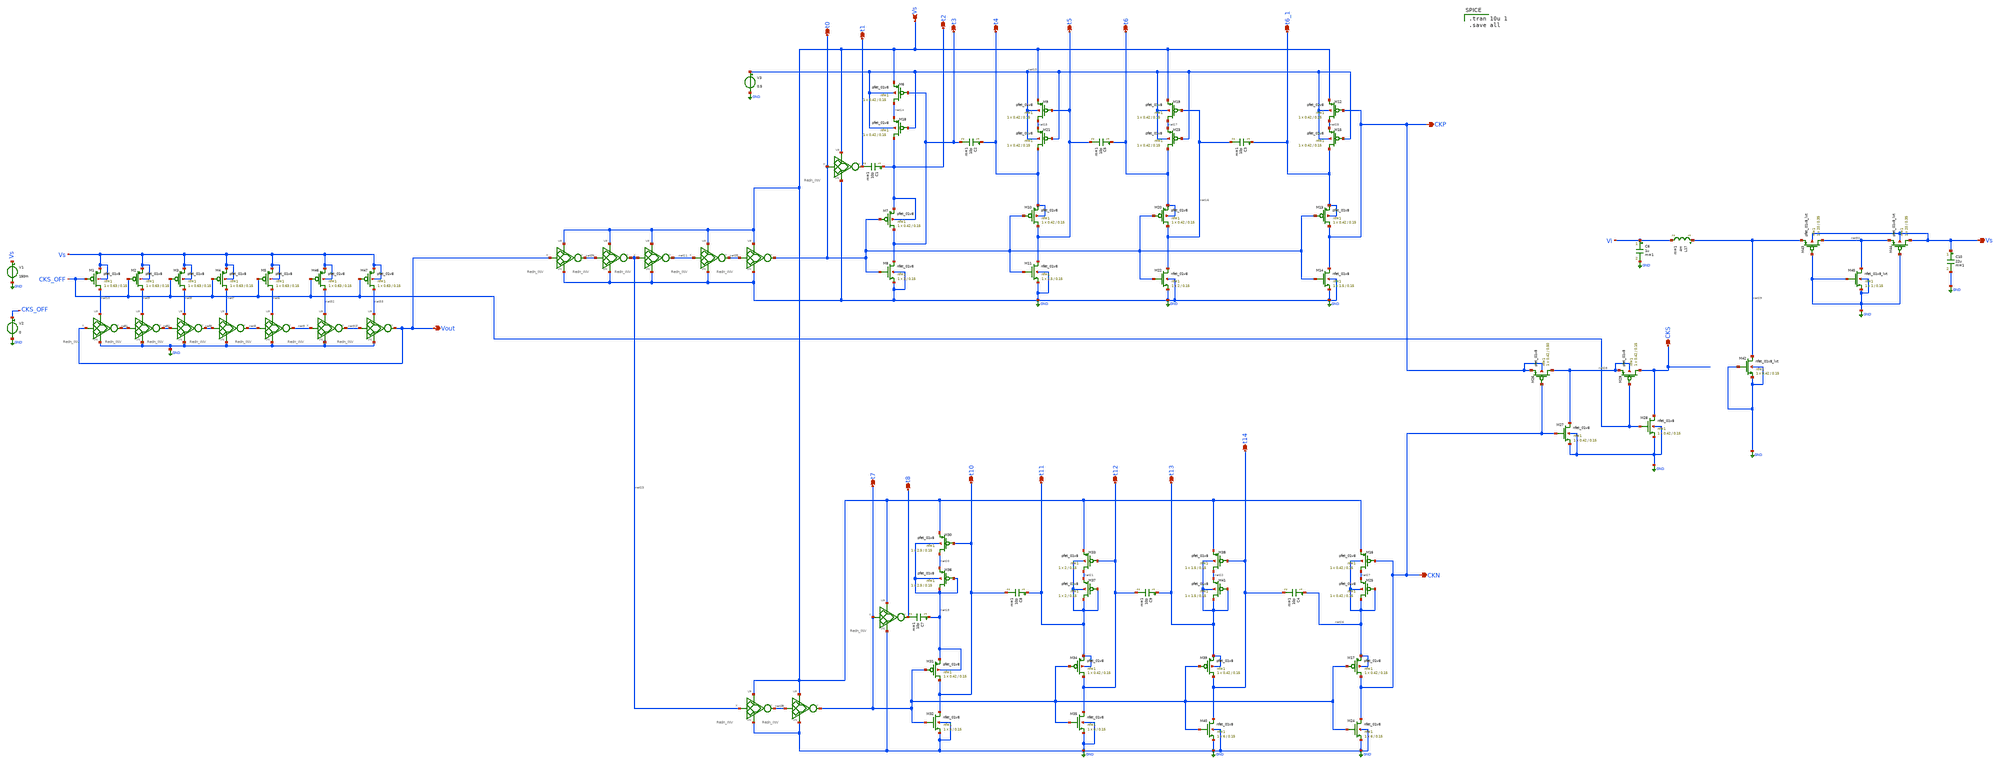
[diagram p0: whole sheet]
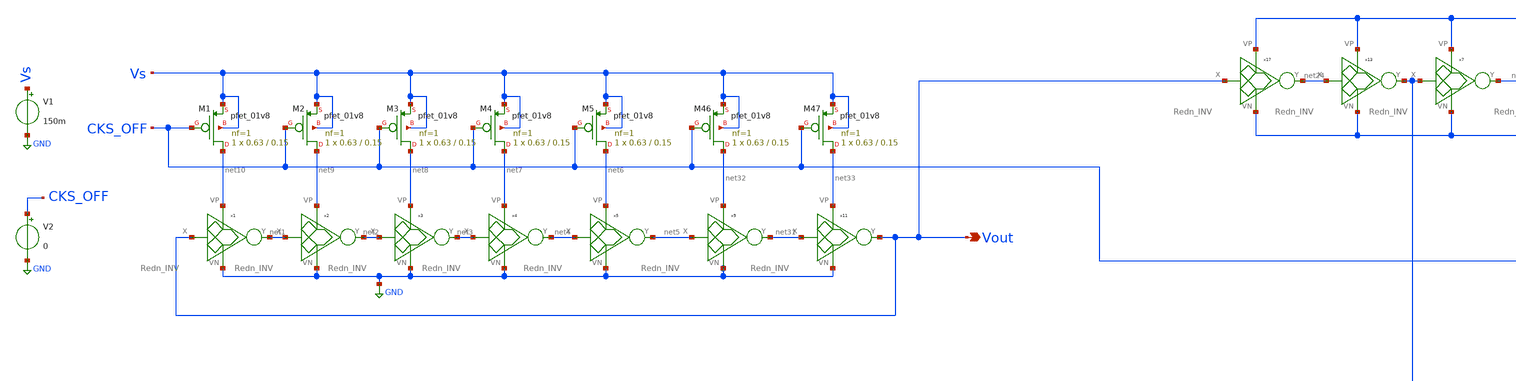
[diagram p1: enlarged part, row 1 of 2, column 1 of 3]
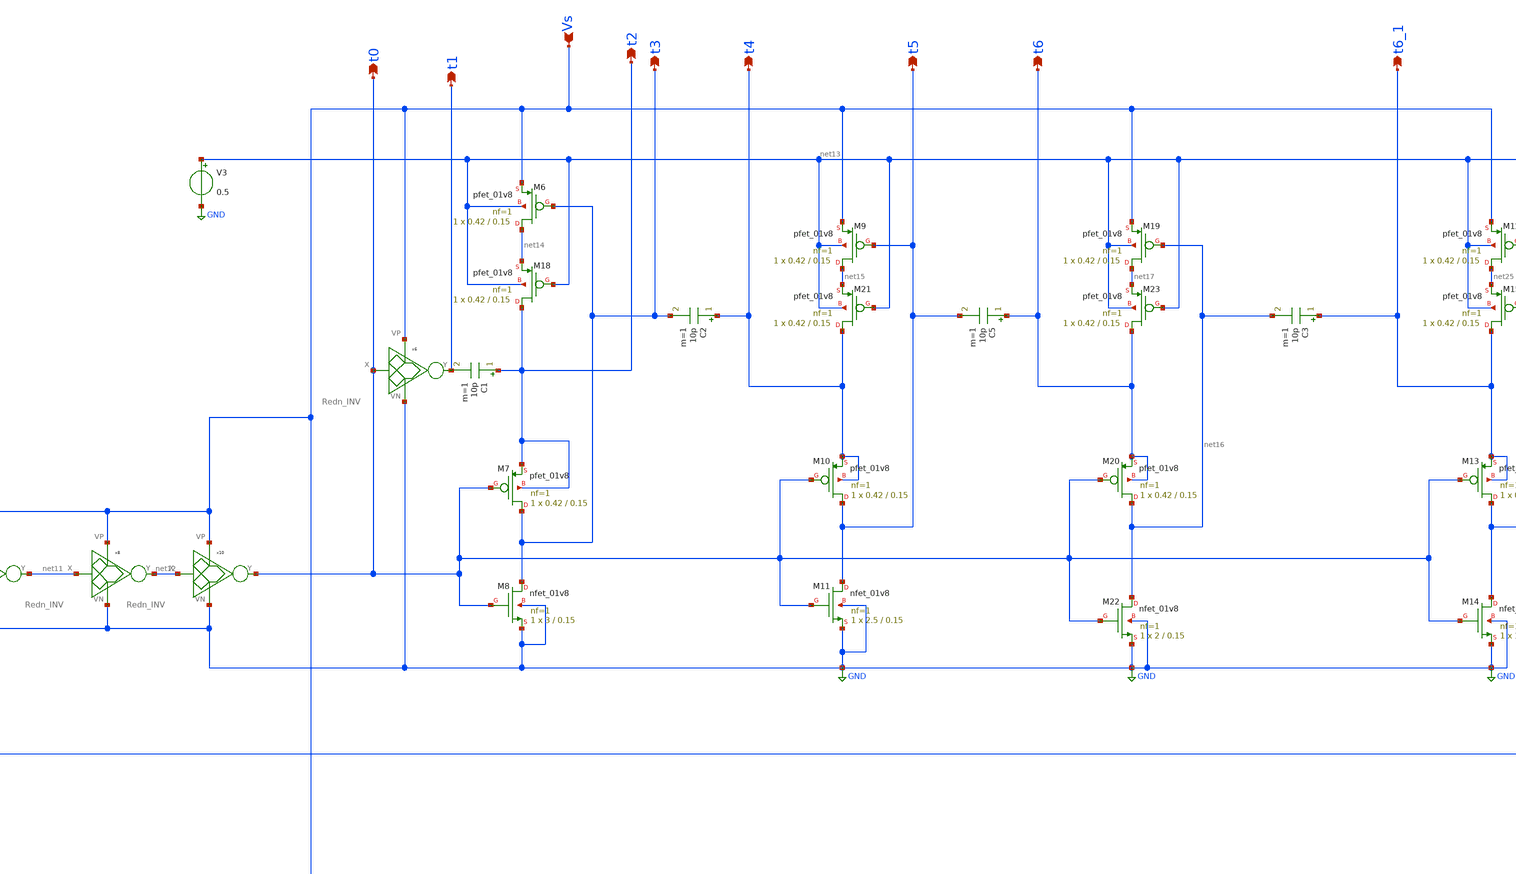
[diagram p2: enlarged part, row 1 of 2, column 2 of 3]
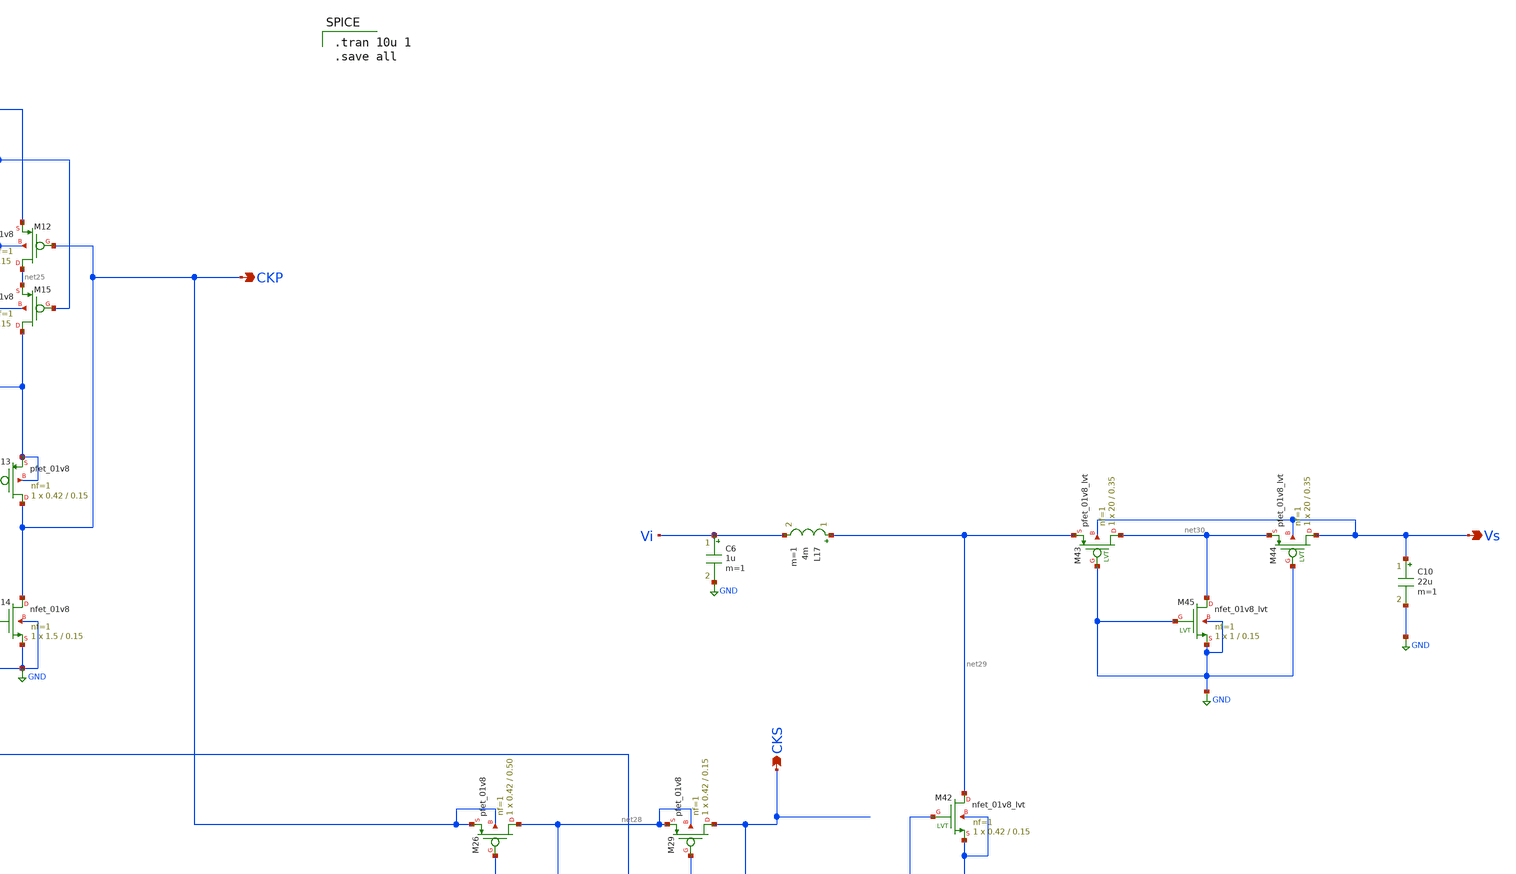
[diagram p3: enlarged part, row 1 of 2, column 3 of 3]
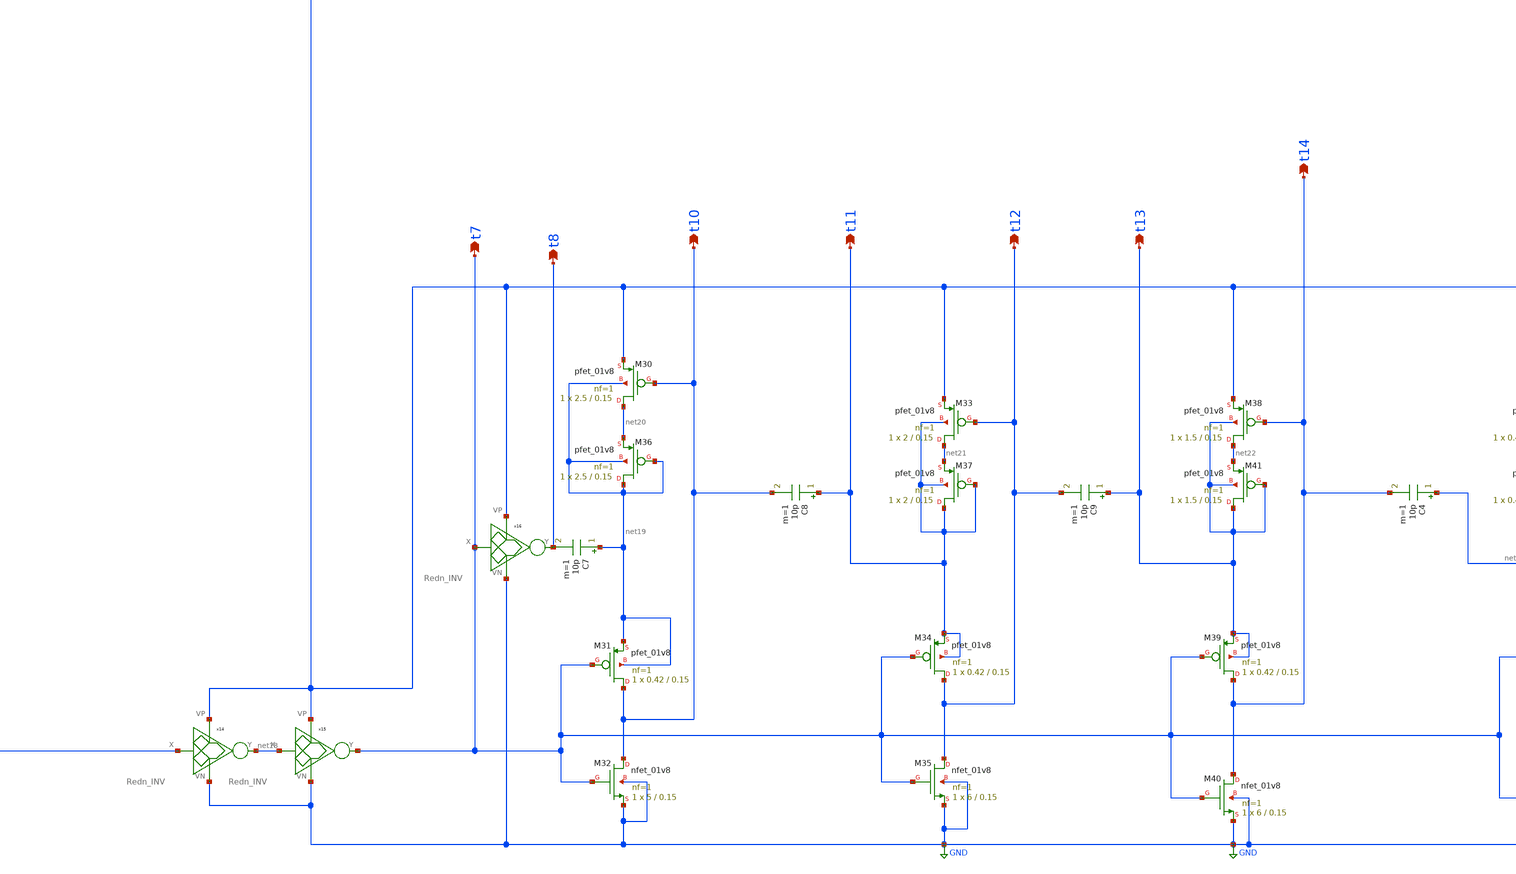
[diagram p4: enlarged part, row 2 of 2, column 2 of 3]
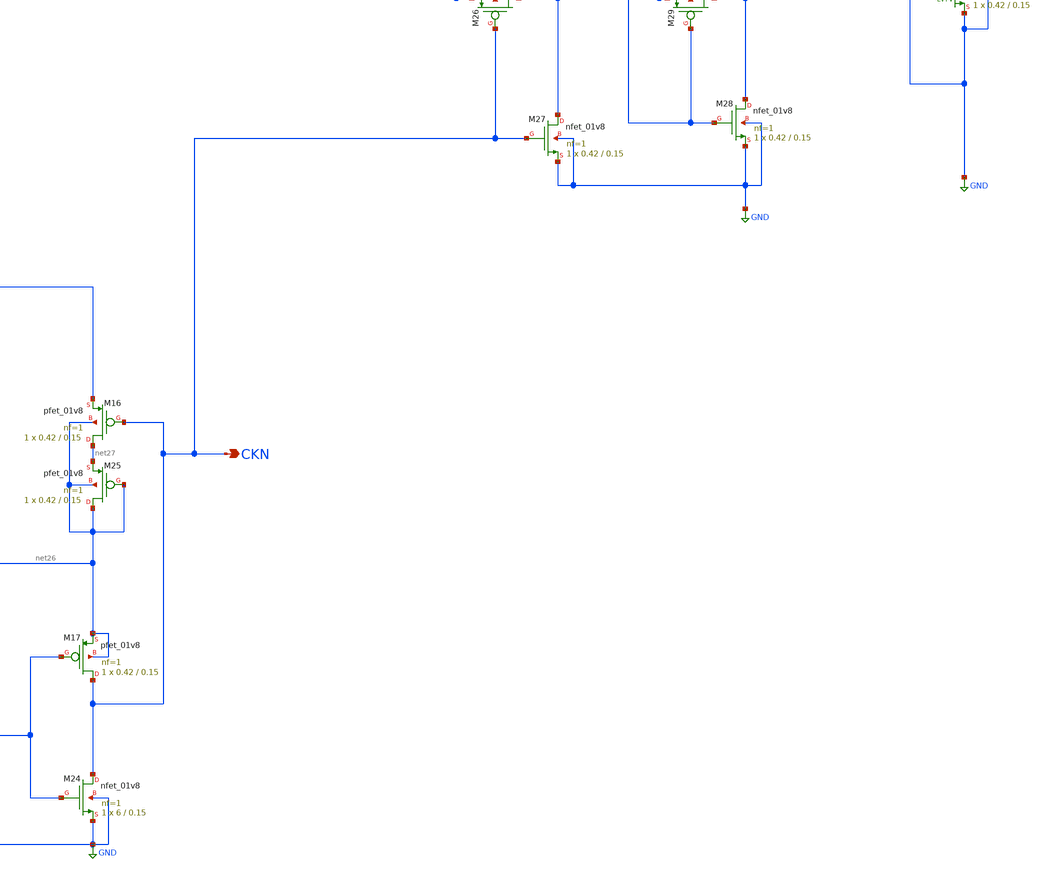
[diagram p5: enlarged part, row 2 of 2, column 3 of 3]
** sch_path: Blocks/Startup Converter/Startup_Conv_3.sch
**.subckt Startup_Conv_3 Vout Vs t2 t3 t4 t1 t0 t6 t5 t10 t11 t8 t7 t13 t12 CKP t6_1 CKN t14 CKS Vs
*.opin Vout
*.ipin Vs
*.opin t2
*.opin t3
*.opin t4
*.opin t1
*.opin t0
*.opin t6
*.opin t5
*.opin t10
*.opin t11
*.opin t8
*.opin t7
*.opin t13
*.opin t12
*.opin CKP
*.opin t6_1
*.opin CKN
*.opin t14
*.opin CKS
*.opin Vs
V1 Vs GND 150m
XM1 net10 CKS_OFF Vs Vs sky130_fd_pr__pfet_01v8 L=0.15 W=0.63 nf=1 ad='int((nf+1)/2) * W/nf * 0.29' as='int((nf+2)/2) * W/nf * 0.29'
+ pd='2*int((nf+1)/2) * (W/nf + 0.29)' ps='2*int((nf+2)/2) * (W/nf + 0.29)' nrd='0.29 / W' nrs='0.29 / W'
+ sa=0 sb=0 sd=0 mult=1 m=1
XM2 net9 CKS_OFF Vs Vs sky130_fd_pr__pfet_01v8 L=0.15 W=0.63 nf=1 ad='int((nf+1)/2) * W/nf * 0.29' as='int((nf+2)/2) * W/nf * 0.29'
+ pd='2*int((nf+1)/2) * (W/nf + 0.29)' ps='2*int((nf+2)/2) * (W/nf + 0.29)' nrd='0.29 / W' nrs='0.29 / W'
+ sa=0 sb=0 sd=0 mult=1 m=1
XM3 net8 CKS_OFF Vs Vs sky130_fd_pr__pfet_01v8 L=0.15 W=0.63 nf=1 ad='int((nf+1)/2) * W/nf * 0.29' as='int((nf+2)/2) * W/nf * 0.29'
+ pd='2*int((nf+1)/2) * (W/nf + 0.29)' ps='2*int((nf+2)/2) * (W/nf + 0.29)' nrd='0.29 / W' nrs='0.29 / W'
+ sa=0 sb=0 sd=0 mult=1 m=1
XM4 net7 CKS_OFF Vs Vs sky130_fd_pr__pfet_01v8 L=0.15 W=0.63 nf=1 ad='int((nf+1)/2) * W/nf * 0.29' as='int((nf+2)/2) * W/nf * 0.29'
+ pd='2*int((nf+1)/2) * (W/nf + 0.29)' ps='2*int((nf+2)/2) * (W/nf + 0.29)' nrd='0.29 / W' nrs='0.29 / W'
+ sa=0 sb=0 sd=0 mult=1 m=1
XM5 net6 CKS_OFF Vs Vs sky130_fd_pr__pfet_01v8 L=0.15 W=0.63 nf=1 ad='int((nf+1)/2) * W/nf * 0.29' as='int((nf+2)/2) * W/nf * 0.29'
+ pd='2*int((nf+1)/2) * (W/nf + 0.29)' ps='2*int((nf+2)/2) * (W/nf + 0.29)' nrd='0.29 / W' nrs='0.29 / W'
+ sa=0 sb=0 sd=0 mult=1 m=1
V2 CKS_OFF GND 0
x1 Vout net1 net10 GND Redn_INV
x2 net1 net2 net9 GND Redn_INV
x3 net2 net3 net8 GND Redn_INV
x4 net3 net4 net7 GND Redn_INV
x5 net4 net5 net6 GND Redn_INV
C1 t2 t1 10p m=1
XM6 net14 t3 Vs net13 sky130_fd_pr__pfet_01v8 L=0.15 W=0.42 nf=1 ad='int((nf+1)/2) * W/nf * 0.29' as='int((nf+2)/2) * W/nf * 0.29'
+ pd='2*int((nf+1)/2) * (W/nf + 0.29)' ps='2*int((nf+2)/2) * (W/nf + 0.29)' nrd='0.29 / W' nrs='0.29 / W'
+ sa=0 sb=0 sd=0 mult=1 m=1
XM7 t3 t0 t2 t2 sky130_fd_pr__pfet_01v8 L=0.15 W=0.42 nf=1 ad='int((nf+1)/2) * W/nf * 0.29' as='int((nf+2)/2) * W/nf * 0.29'
+ pd='2*int((nf+1)/2) * (W/nf + 0.29)' ps='2*int((nf+2)/2) * (W/nf + 0.29)' nrd='0.29 / W' nrs='0.29 / W'
+ sa=0 sb=0 sd=0 mult=1 m=1
XM8 t3 t0 GND GND sky130_fd_pr__nfet_01v8 L=0.15 W=3 nf=1 ad='int((nf+1)/2) * W/nf * 0.29' as='int((nf+2)/2) * W/nf * 0.29'
+ pd='2*int((nf+1)/2) * (W/nf + 0.29)' ps='2*int((nf+2)/2) * (W/nf + 0.29)' nrd='0.29 / W' nrs='0.29 / W'
+ sa=0 sb=0 sd=0 mult=1 m=1
XM9 net15 t5 Vs net13 sky130_fd_pr__pfet_01v8 L=0.15 W=0.42 nf=1 ad='int((nf+1)/2) * W/nf * 0.29' as='int((nf+2)/2) * W/nf * 0.29'
+ pd='2*int((nf+1)/2) * (W/nf + 0.29)' ps='2*int((nf+2)/2) * (W/nf + 0.29)' nrd='0.29 / W' nrs='0.29 / W'
+ sa=0 sb=0 sd=0 mult=1 m=1
XM10 t5 t0 t4 t4 sky130_fd_pr__pfet_01v8 L=0.15 W=0.42 nf=1 ad='int((nf+1)/2) * W/nf * 0.29' as='int((nf+2)/2) * W/nf * 0.29'
+ pd='2*int((nf+1)/2) * (W/nf + 0.29)' ps='2*int((nf+2)/2) * (W/nf + 0.29)' nrd='0.29 / W' nrs='0.29 / W'
+ sa=0 sb=0 sd=0 mult=1 m=1
XM11 t5 t0 GND GND sky130_fd_pr__nfet_01v8 L=0.15 W=2.5 nf=1 ad='int((nf+1)/2) * W/nf * 0.29' as='int((nf+2)/2) * W/nf * 0.29'
+ pd='2*int((nf+1)/2) * (W/nf + 0.29)' ps='2*int((nf+2)/2) * (W/nf + 0.29)' nrd='0.29 / W' nrs='0.29 / W'
+ sa=0 sb=0 sd=0 mult=1 m=1
XM18 t2 net13 net14 net13 sky130_fd_pr__pfet_01v8 L=0.15 W=0.42 nf=1 ad='int((nf+1)/2) * W/nf * 0.29'
+ as='int((nf+2)/2) * W/nf * 0.29' pd='2*int((nf+1)/2) * (W/nf + 0.29)' ps='2*int((nf+2)/2) * (W/nf + 0.29)'
+ nrd='0.29 / W' nrs='0.29 / W' sa=0 sb=0 sd=0 mult=1 m=1
XM21 t4 net13 net15 net13 sky130_fd_pr__pfet_01v8 L=0.15 W=0.42 nf=1 ad='int((nf+1)/2) * W/nf * 0.29'
+ as='int((nf+2)/2) * W/nf * 0.29' pd='2*int((nf+1)/2) * (W/nf + 0.29)' ps='2*int((nf+2)/2) * (W/nf + 0.29)'
+ nrd='0.29 / W' nrs='0.29 / W' sa=0 sb=0 sd=0 mult=1 m=1
C2 t4 t3 10p m=1
x7 net23 net11 Vs GND Redn_INV
x8 net11 net12 Vs GND Redn_INV
x10 net12 t0 Vs GND Redn_INV
x6 t0 t1 Vs GND Redn_INV
XM19 net17 net16 Vs net13 sky130_fd_pr__pfet_01v8 L=0.15 W=0.42 nf=1 ad='int((nf+1)/2) * W/nf * 0.29'
+ as='int((nf+2)/2) * W/nf * 0.29' pd='2*int((nf+1)/2) * (W/nf + 0.29)' ps='2*int((nf+2)/2) * (W/nf + 0.29)'
+ nrd='0.29 / W' nrs='0.29 / W' sa=0 sb=0 sd=0 mult=1 m=1
XM20 net16 t0 t6 t6 sky130_fd_pr__pfet_01v8 L=0.15 W=0.42 nf=1 ad='int((nf+1)/2) * W/nf * 0.29' as='int((nf+2)/2) * W/nf * 0.29'
+ pd='2*int((nf+1)/2) * (W/nf + 0.29)' ps='2*int((nf+2)/2) * (W/nf + 0.29)' nrd='0.29 / W' nrs='0.29 / W'
+ sa=0 sb=0 sd=0 mult=1 m=1
XM22 net16 t0 GND GND sky130_fd_pr__nfet_01v8 L=0.15 W=2 nf=1 ad='int((nf+1)/2) * W/nf * 0.29' as='int((nf+2)/2) * W/nf * 0.29'
+ pd='2*int((nf+1)/2) * (W/nf + 0.29)' ps='2*int((nf+2)/2) * (W/nf + 0.29)' nrd='0.29 / W' nrs='0.29 / W'
+ sa=0 sb=0 sd=0 mult=1 m=1
XM23 t6 net13 net17 net13 sky130_fd_pr__pfet_01v8 L=0.15 W=0.42 nf=1 ad='int((nf+1)/2) * W/nf * 0.29'
+ as='int((nf+2)/2) * W/nf * 0.29' pd='2*int((nf+1)/2) * (W/nf + 0.29)' ps='2*int((nf+2)/2) * (W/nf + 0.29)'
+ nrd='0.29 / W' nrs='0.29 / W' sa=0 sb=0 sd=0 mult=1 m=1
C5 t6 t5 10p m=1
C7 net19 t8 10p m=1
XM30 net20 t10 Vs net19 sky130_fd_pr__pfet_01v8 L=0.15 W=2.5 nf=1 ad='int((nf+1)/2) * W/nf * 0.29' as='int((nf+2)/2) * W/nf * 0.29'
+ pd='2*int((nf+1)/2) * (W/nf + 0.29)' ps='2*int((nf+2)/2) * (W/nf + 0.29)' nrd='0.29 / W' nrs='0.29 / W'
+ sa=0 sb=0 sd=0 mult=1 m=1
XM31 t10 t7 net19 net19 sky130_fd_pr__pfet_01v8 L=0.15 W=0.42 nf=1 ad='int((nf+1)/2) * W/nf * 0.29' as='int((nf+2)/2) * W/nf * 0.29'
+ pd='2*int((nf+1)/2) * (W/nf + 0.29)' ps='2*int((nf+2)/2) * (W/nf + 0.29)' nrd='0.29 / W' nrs='0.29 / W'
+ sa=0 sb=0 sd=0 mult=1 m=1
XM32 t10 t7 GND GND sky130_fd_pr__nfet_01v8 L=0.15 W=5 nf=1 ad='int((nf+1)/2) * W/nf * 0.29' as='int((nf+2)/2) * W/nf * 0.29'
+ pd='2*int((nf+1)/2) * (W/nf + 0.29)' ps='2*int((nf+2)/2) * (W/nf + 0.29)' nrd='0.29 / W' nrs='0.29 / W'
+ sa=0 sb=0 sd=0 mult=1 m=1
XM33 net21 t12 Vs t11 sky130_fd_pr__pfet_01v8 L=0.15 W=2 nf=1 ad='int((nf+1)/2) * W/nf * 0.29' as='int((nf+2)/2) * W/nf * 0.29'
+ pd='2*int((nf+1)/2) * (W/nf + 0.29)' ps='2*int((nf+2)/2) * (W/nf + 0.29)' nrd='0.29 / W' nrs='0.29 / W'
+ sa=0 sb=0 sd=0 mult=1 m=1
XM34 t12 t7 t11 t11 sky130_fd_pr__pfet_01v8 L=0.15 W=0.42 nf=1 ad='int((nf+1)/2) * W/nf * 0.29' as='int((nf+2)/2) * W/nf * 0.29'
+ pd='2*int((nf+1)/2) * (W/nf + 0.29)' ps='2*int((nf+2)/2) * (W/nf + 0.29)' nrd='0.29 / W' nrs='0.29 / W'
+ sa=0 sb=0 sd=0 mult=1 m=1
XM35 t12 t7 GND GND sky130_fd_pr__nfet_01v8 L=0.15 W=6 nf=1 ad='int((nf+1)/2) * W/nf * 0.29' as='int((nf+2)/2) * W/nf * 0.29'
+ pd='2*int((nf+1)/2) * (W/nf + 0.29)' ps='2*int((nf+2)/2) * (W/nf + 0.29)' nrd='0.29 / W' nrs='0.29 / W'
+ sa=0 sb=0 sd=0 mult=1 m=1
XM36 net19 net19 net20 net19 sky130_fd_pr__pfet_01v8 L=0.15 W=2.5 nf=1 ad='int((nf+1)/2) * W/nf * 0.29'
+ as='int((nf+2)/2) * W/nf * 0.29' pd='2*int((nf+1)/2) * (W/nf + 0.29)' ps='2*int((nf+2)/2) * (W/nf + 0.29)'
+ nrd='0.29 / W' nrs='0.29 / W' sa=0 sb=0 sd=0 mult=1 m=1
XM37 t11 t11 net21 t11 sky130_fd_pr__pfet_01v8 L=0.15 W=2 nf=1 ad='int((nf+1)/2) * W/nf * 0.29' as='int((nf+2)/2) * W/nf * 0.29'
+ pd='2*int((nf+1)/2) * (W/nf + 0.29)' ps='2*int((nf+2)/2) * (W/nf + 0.29)' nrd='0.29 / W' nrs='0.29 / W'
+ sa=0 sb=0 sd=0 mult=1 m=1
C8 t11 t10 10p m=1
x14 net23 net18 Vs GND Redn_INV
x15 net18 t7 Vs GND Redn_INV
x16 t7 t8 Vs GND Redn_INV
XM38 net22 t14 Vs t13 sky130_fd_pr__pfet_01v8 L=0.15 W=1.5 nf=1 ad='int((nf+1)/2) * W/nf * 0.29' as='int((nf+2)/2) * W/nf * 0.29'
+ pd='2*int((nf+1)/2) * (W/nf + 0.29)' ps='2*int((nf+2)/2) * (W/nf + 0.29)' nrd='0.29 / W' nrs='0.29 / W'
+ sa=0 sb=0 sd=0 mult=1 m=1
XM39 t14 t7 t13 t13 sky130_fd_pr__pfet_01v8 L=0.15 W=0.42 nf=1 ad='int((nf+1)/2) * W/nf * 0.29' as='int((nf+2)/2) * W/nf * 0.29'
+ pd='2*int((nf+1)/2) * (W/nf + 0.29)' ps='2*int((nf+2)/2) * (W/nf + 0.29)' nrd='0.29 / W' nrs='0.29 / W'
+ sa=0 sb=0 sd=0 mult=1 m=1
XM40 t14 t7 GND GND sky130_fd_pr__nfet_01v8 L=0.15 W=6 nf=1 ad='int((nf+1)/2) * W/nf * 0.29' as='int((nf+2)/2) * W/nf * 0.29'
+ pd='2*int((nf+1)/2) * (W/nf + 0.29)' ps='2*int((nf+2)/2) * (W/nf + 0.29)' nrd='0.29 / W' nrs='0.29 / W'
+ sa=0 sb=0 sd=0 mult=1 m=1
XM41 t13 t13 net22 t13 sky130_fd_pr__pfet_01v8 L=0.15 W=1.5 nf=1 ad='int((nf+1)/2) * W/nf * 0.29' as='int((nf+2)/2) * W/nf * 0.29'
+ pd='2*int((nf+1)/2) * (W/nf + 0.29)' ps='2*int((nf+2)/2) * (W/nf + 0.29)' nrd='0.29 / W' nrs='0.29 / W'
+ sa=0 sb=0 sd=0 mult=1 m=1
C9 t13 t12 10p m=1
x13 net24 net23 Vs GND Redn_INV
x17 Vout net24 Vs GND Redn_INV
XM12 net25 CKP Vs net13 sky130_fd_pr__pfet_01v8 L=0.15 W=0.42 nf=1 ad='int((nf+1)/2) * W/nf * 0.29' as='int((nf+2)/2) * W/nf * 0.29'
+ pd='2*int((nf+1)/2) * (W/nf + 0.29)' ps='2*int((nf+2)/2) * (W/nf + 0.29)' nrd='0.29 / W' nrs='0.29 / W'
+ sa=0 sb=0 sd=0 mult=1 m=1
XM13 CKP t0 t6_1 t6_1 sky130_fd_pr__pfet_01v8 L=0.15 W=0.42 nf=1 ad='int((nf+1)/2) * W/nf * 0.29' as='int((nf+2)/2) * W/nf * 0.29'
+ pd='2*int((nf+1)/2) * (W/nf + 0.29)' ps='2*int((nf+2)/2) * (W/nf + 0.29)' nrd='0.29 / W' nrs='0.29 / W'
+ sa=0 sb=0 sd=0 mult=1 m=1
XM14 CKP t0 GND GND sky130_fd_pr__nfet_01v8 L=0.15 W=1.5 nf=1 ad='int((nf+1)/2) * W/nf * 0.29' as='int((nf+2)/2) * W/nf * 0.29'
+ pd='2*int((nf+1)/2) * (W/nf + 0.29)' ps='2*int((nf+2)/2) * (W/nf + 0.29)' nrd='0.29 / W' nrs='0.29 / W'
+ sa=0 sb=0 sd=0 mult=1 m=1
XM15 t6_1 net13 net25 net13 sky130_fd_pr__pfet_01v8 L=0.15 W=0.42 nf=1 ad='int((nf+1)/2) * W/nf * 0.29'
+ as='int((nf+2)/2) * W/nf * 0.29' pd='2*int((nf+1)/2) * (W/nf + 0.29)' ps='2*int((nf+2)/2) * (W/nf + 0.29)'
+ nrd='0.29 / W' nrs='0.29 / W' sa=0 sb=0 sd=0 mult=1 m=1
C3 t6_1 net16 10p m=1
XM16 net27 CKN Vs net26 sky130_fd_pr__pfet_01v8 L=0.15 W=0.42 nf=1 ad='int((nf+1)/2) * W/nf * 0.29' as='int((nf+2)/2) * W/nf * 0.29'
+ pd='2*int((nf+1)/2) * (W/nf + 0.29)' ps='2*int((nf+2)/2) * (W/nf + 0.29)' nrd='0.29 / W' nrs='0.29 / W'
+ sa=0 sb=0 sd=0 mult=1 m=1
XM17 CKN t7 net26 net26 sky130_fd_pr__pfet_01v8 L=0.15 W=0.42 nf=1 ad='int((nf+1)/2) * W/nf * 0.29' as='int((nf+2)/2) * W/nf * 0.29'
+ pd='2*int((nf+1)/2) * (W/nf + 0.29)' ps='2*int((nf+2)/2) * (W/nf + 0.29)' nrd='0.29 / W' nrs='0.29 / W'
+ sa=0 sb=0 sd=0 mult=1 m=1
XM24 CKN t7 GND GND sky130_fd_pr__nfet_01v8 L=0.15 W=6 nf=1 ad='int((nf+1)/2) * W/nf * 0.29' as='int((nf+2)/2) * W/nf * 0.29'
+ pd='2*int((nf+1)/2) * (W/nf + 0.29)' ps='2*int((nf+2)/2) * (W/nf + 0.29)' nrd='0.29 / W' nrs='0.29 / W'
+ sa=0 sb=0 sd=0 mult=1 m=1
XM25 net26 net26 net27 net26 sky130_fd_pr__pfet_01v8 L=0.15 W=0.42 nf=1 ad='int((nf+1)/2) * W/nf * 0.29'
+ as='int((nf+2)/2) * W/nf * 0.29' pd='2*int((nf+1)/2) * (W/nf + 0.29)' ps='2*int((nf+2)/2) * (W/nf + 0.29)'
+ nrd='0.29 / W' nrs='0.29 / W' sa=0 sb=0 sd=0 mult=1 m=1
C4 net26 t14 10p m=1
XM26 net28 CKN CKP CKP sky130_fd_pr__pfet_01v8 L=0.50 W=0.42 nf=1 ad='int((nf+1)/2) * W/nf * 0.29' as='int((nf+2)/2) * W/nf * 0.29'
+ pd='2*int((nf+1)/2) * (W/nf + 0.29)' ps='2*int((nf+2)/2) * (W/nf + 0.29)' nrd='0.29 / W' nrs='0.29 / W'
+ sa=0 sb=0 sd=0 mult=1 m=1
XM27 net28 CKN GND GND sky130_fd_pr__nfet_01v8 L=0.15 W=0.42 nf=1 ad='int((nf+1)/2) * W/nf * 0.29' as='int((nf+2)/2) * W/nf * 0.29'
+ pd='2*int((nf+1)/2) * (W/nf + 0.29)' ps='2*int((nf+2)/2) * (W/nf + 0.29)' nrd='0.29 / W' nrs='0.29 / W'
+ sa=0 sb=0 sd=0 mult=1 m=1
XM28 CKS CKS_OFF GND GND sky130_fd_pr__nfet_01v8 L=0.15 W=0.42 nf=1 ad='int((nf+1)/2) * W/nf * 0.29'
+ as='int((nf+2)/2) * W/nf * 0.29' pd='2*int((nf+1)/2) * (W/nf + 0.29)' ps='2*int((nf+2)/2) * (W/nf + 0.29)'
+ nrd='0.29 / W' nrs='0.29 / W' sa=0 sb=0 sd=0 mult=1 m=1
XM29 CKS CKS_OFF net28 net28 sky130_fd_pr__pfet_01v8 L=0.15 W=0.42 nf=1 ad='int((nf+1)/2) * W/nf * 0.29'
+ as='int((nf+2)/2) * W/nf * 0.29' pd='2*int((nf+1)/2) * (W/nf + 0.29)' ps='2*int((nf+2)/2) * (W/nf + 0.29)'
+ nrd='0.29 / W' nrs='0.29 / W' sa=0 sb=0 sd=0 mult=1 m=1
C6 Vi GND 1u m=1
L17 net29 Vi 4m m=1
C10 Vs GND 22u m=1
XM42 net29 GND GND GND sky130_fd_pr__nfet_01v8_lvt L=0.15 W=0.42 nf=1 ad='int((nf+1)/2) * W/nf * 0.29'
+ as='int((nf+2)/2) * W/nf * 0.29' pd='2*int((nf+1)/2) * (W/nf + 0.29)' ps='2*int((nf+2)/2) * (W/nf + 0.29)'
+ nrd='0.29 / W' nrs='0.29 / W' sa=0 sb=0 sd=0 mult=1 m=1
XM43 net30 GND net29 Vs sky130_fd_pr__pfet_01v8_lvt L=0.35 W=20 nf=1 ad='int((nf+1)/2) * W/nf * 0.29'
+ as='int((nf+2)/2) * W/nf * 0.29' pd='2*int((nf+1)/2) * (W/nf + 0.29)' ps='2*int((nf+2)/2) * (W/nf + 0.29)'
+ nrd='0.29 / W' nrs='0.29 / W' sa=0 sb=0 sd=0 mult=1 m=1
XM44 Vs GND net30 Vs sky130_fd_pr__pfet_01v8_lvt L=0.35 W=20 nf=1 ad='int((nf+1)/2) * W/nf * 0.29' as='int((nf+2)/2) * W/nf * 0.29'
+ pd='2*int((nf+1)/2) * (W/nf + 0.29)' ps='2*int((nf+2)/2) * (W/nf + 0.29)' nrd='0.29 / W' nrs='0.29 / W'
+ sa=0 sb=0 sd=0 mult=1 m=1
XM45 net30 GND GND GND sky130_fd_pr__nfet_01v8_lvt L=0.15 W=1 nf=1 ad='int((nf+1)/2) * W/nf * 0.29' as='int((nf+2)/2) * W/nf * 0.29'
+ pd='2*int((nf+1)/2) * (W/nf + 0.29)' ps='2*int((nf+2)/2) * (W/nf + 0.29)' nrd='0.29 / W' nrs='0.29 / W'
+ sa=0 sb=0 sd=0 mult=1 m=1
x9 net5 net31 net32 GND Redn_INV
x11 net31 Vout net33 GND Redn_INV
XM46 net32 CKS_OFF Vs Vs sky130_fd_pr__pfet_01v8 L=0.15 W=0.63 nf=1 ad='int((nf+1)/2) * W/nf * 0.29'
+ as='int((nf+2)/2) * W/nf * 0.29' pd='2*int((nf+1)/2) * (W/nf + 0.29)' ps='2*int((nf+2)/2) * (W/nf + 0.29)'
+ nrd='0.29 / W' nrs='0.29 / W' sa=0 sb=0 sd=0 mult=1 m=1
XM47 net33 CKS_OFF Vs Vs sky130_fd_pr__pfet_01v8 L=0.15 W=0.63 nf=1 ad='int((nf+1)/2) * W/nf * 0.29'
+ as='int((nf+2)/2) * W/nf * 0.29' pd='2*int((nf+1)/2) * (W/nf + 0.29)' ps='2*int((nf+2)/2) * (W/nf + 0.29)'
+ nrd='0.29 / W' nrs='0.29 / W' sa=0 sb=0 sd=0 mult=1 m=1
V3 net13 GND 0.5
**** begin user architecture code

** opencircuitdesign pdks install
.lib $::SKYWATER_MODELS/sky130.lib.spice tt



.tran 10u 1
.save all

**** end user architecture code
**.ends

* expanding   symbol:  component/Reduntant_Inverter/Redn_INV.sym # of pins=4
** sym_path: component/Reduntant_Inverter/Redn_INV.sym
** sch_path: component/Reduntant_Inverter/Redn_INV.sch
.subckt Redn_INV X Y VP VN
*.opin Y
*.ipin X
*.iopin VP
*.iopin VN
XM15 net4 X VN VN sky130_fd_pr__nfet_01v8_lvt L=0.15 W=1 nf=1 ad='int((nf+1)/2) * W/nf * 0.29' as='int((nf+2)/2) * W/nf * 0.29'
+ pd='2*int((nf+1)/2) * (W/nf + 0.29)' ps='2*int((nf+2)/2) * (W/nf + 0.29)' nrd='0.29 / W' nrs='0.29 / W'
+ sa=0 sb=0 sd=0 mult=1 m=1
XM1 net5 X net3 VN sky130_fd_pr__nfet_01v8_lvt L=0.15 W=3.25 nf=1 ad='int((nf+1)/2) * W/nf * 0.29' as='int((nf+2)/2) * W/nf * 0.29'
+ pd='2*int((nf+1)/2) * (W/nf + 0.29)' ps='2*int((nf+2)/2) * (W/nf + 0.29)' nrd='0.29 / W' nrs='0.29 / W'
+ sa=0 sb=0 sd=0 mult=1 m=1
XM16 Y X net6 VN sky130_fd_pr__nfet_01v8_lvt L=0.15 W=6.5 nf=1 ad='int((nf+1)/2) * W/nf * 0.29' as='int((nf+2)/2) * W/nf * 0.29'
+ pd='2*int((nf+1)/2) * (W/nf + 0.29)' ps='2*int((nf+2)/2) * (W/nf + 0.29)' nrd='0.29 / W' nrs='0.29 / W'
+ sa=0 sb=0 sd=0 mult=1 m=1
XM17 net3 X VN VN sky130_fd_pr__nfet_01v8_lvt L=0.15 W=3.25 nf=1 ad='int((nf+1)/2) * W/nf * 0.29' as='int((nf+2)/2) * W/nf * 0.29'
+ pd='2*int((nf+1)/2) * (W/nf + 0.29)' ps='2*int((nf+2)/2) * (W/nf + 0.29)' nrd='0.29 / W' nrs='0.29 / W'
+ sa=0 sb=0 sd=0 mult=1 m=1
XM18 net2 X VN VN sky130_fd_pr__nfet_01v8_lvt L=0.15 W=1.5 nf=1 ad='int((nf+1)/2) * W/nf * 0.29' as='int((nf+2)/2) * W/nf * 0.29'
+ pd='2*int((nf+1)/2) * (W/nf + 0.29)' ps='2*int((nf+2)/2) * (W/nf + 0.29)' nrd='0.29 / W' nrs='0.29 / W'
+ sa=0 sb=0 sd=0 mult=1 m=1
XM19 net1 X VN VN sky130_fd_pr__nfet_01v8_lvt L=0.15 W=6.5 nf=1 ad='int((nf+1)/2) * W/nf * 0.29' as='int((nf+2)/2) * W/nf * 0.29'
+ pd='2*int((nf+1)/2) * (W/nf + 0.29)' ps='2*int((nf+2)/2) * (W/nf + 0.29)' nrd='0.29 / W' nrs='0.29 / W'
+ sa=0 sb=0 sd=0 mult=1 m=1
XM20 net6 X net1 VN sky130_fd_pr__nfet_01v8_lvt L=0.15 W=6.5 nf=1 ad='int((nf+1)/2) * W/nf * 0.29' as='int((nf+2)/2) * W/nf * 0.29'
+ pd='2*int((nf+1)/2) * (W/nf + 0.29)' ps='2*int((nf+2)/2) * (W/nf + 0.29)' nrd='0.29 / W' nrs='0.29 / W'
+ sa=0 sb=0 sd=0 mult=1 m=1
XM2 net4 X VP VP sky130_fd_pr__pfet_01v8 L=0.15 W=10 nf=1 ad='int((nf+1)/2) * W/nf * 0.29' as='int((nf+2)/2) * W/nf * 0.29'
+ pd='2*int((nf+1)/2) * (W/nf + 0.29)' ps='2*int((nf+2)/2) * (W/nf + 0.29)' nrd='0.29 / W' nrs='0.29 / W'
+ sa=0 sb=0 sd=0 mult=1 m=1
XM5 net5 X net4 net4 sky130_fd_pr__pfet_01v8 L=0.15 W=10 nf=1 ad='int((nf+1)/2) * W/nf * 0.29' as='int((nf+2)/2) * W/nf * 0.29'
+ pd='2*int((nf+1)/2) * (W/nf + 0.29)' ps='2*int((nf+2)/2) * (W/nf + 0.29)' nrd='0.29 / W' nrs='0.29 / W'
+ sa=0 sb=0 sd=0 mult=1 m=1
XM6 Y X net5 VP sky130_fd_pr__pfet_01v8 L=0.15 W=10 nf=1 ad='int((nf+1)/2) * W/nf * 0.29' as='int((nf+2)/2) * W/nf * 0.29'
+ pd='2*int((nf+1)/2) * (W/nf + 0.29)' ps='2*int((nf+2)/2) * (W/nf + 0.29)' nrd='0.29 / W' nrs='0.29 / W'
+ sa=0 sb=0 sd=0 mult=1 m=1
XM8 net3 X VP VP sky130_fd_pr__pfet_01v8 L=0.15 W=2 nf=1 ad='int((nf+1)/2) * W/nf * 0.29' as='int((nf+2)/2) * W/nf * 0.29'
+ pd='2*int((nf+1)/2) * (W/nf + 0.29)' ps='2*int((nf+2)/2) * (W/nf + 0.29)' nrd='0.29 / W' nrs='0.29 / W'
+ sa=0 sb=0 sd=0 mult=1 m=1
XM12 net2 X VP VP sky130_fd_pr__pfet_01v8 L=0.15 W=5 nf=1 ad='int((nf+1)/2) * W/nf * 0.29' as='int((nf+2)/2) * W/nf * 0.29'
+ pd='2*int((nf+1)/2) * (W/nf + 0.29)' ps='2*int((nf+2)/2) * (W/nf + 0.29)' nrd='0.29 / W' nrs='0.29 / W'
+ sa=0 sb=0 sd=0 mult=1 m=1
XM14 net6 X net2 VP sky130_fd_pr__pfet_01v8 L=0.15 W=5 nf=1 ad='int((nf+1)/2) * W/nf * 0.29' as='int((nf+2)/2) * W/nf * 0.29'
+ pd='2*int((nf+1)/2) * (W/nf + 0.29)' ps='2*int((nf+2)/2) * (W/nf + 0.29)' nrd='0.29 / W' nrs='0.29 / W'
+ sa=0 sb=0 sd=0 mult=1 m=1
XM21 net1 X VP VP sky130_fd_pr__pfet_01v8 L=0.15 W=1.5 nf=1 ad='int((nf+1)/2) * W/nf * 0.29' as='int((nf+2)/2) * W/nf * 0.29'
+ pd='2*int((nf+1)/2) * (W/nf + 0.29)' ps='2*int((nf+2)/2) * (W/nf + 0.29)' nrd='0.29 / W' nrs='0.29 / W'
+ sa=0 sb=0 sd=0 mult=1 m=1
.ends

.GLOBAL GND
.end
